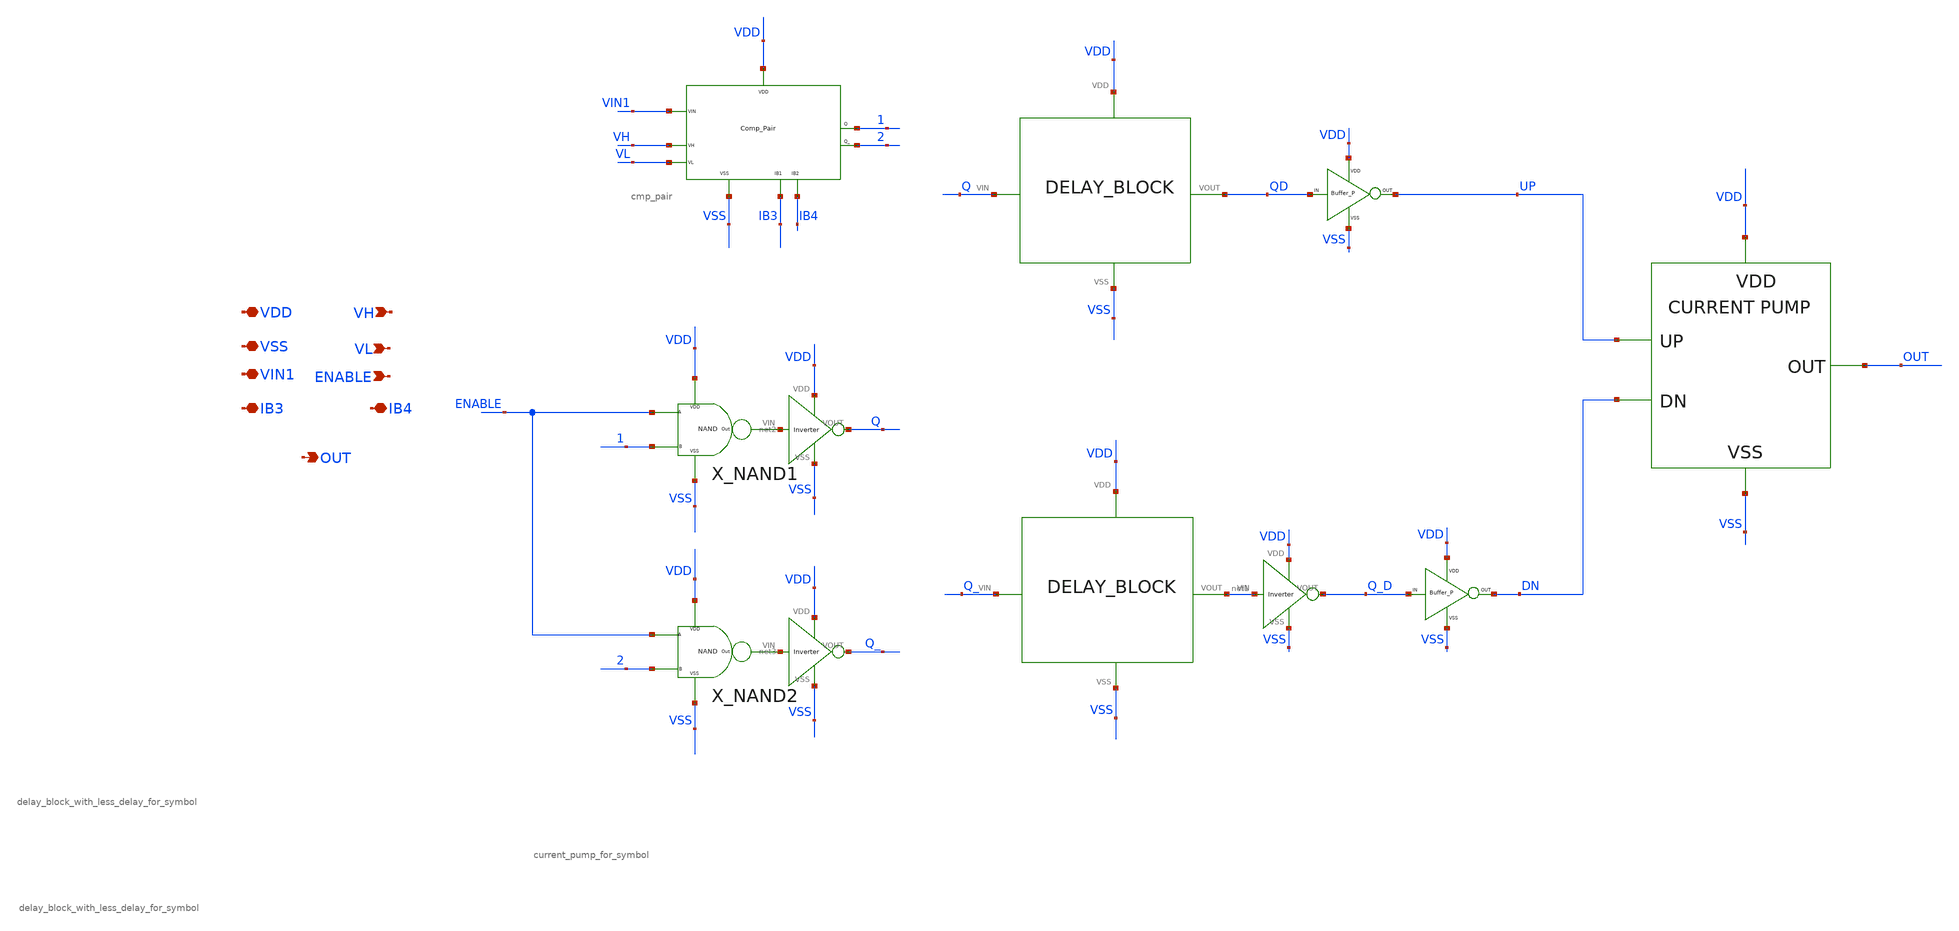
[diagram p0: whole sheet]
** sch_path: xschem/DC_DC_Converter_xschem/OTHERS/DC_DC_Converter_JV11/TOP_LEVEL/Top_Final/Top_2.sch
**.subckt Top_2 VDD VSS OUT VH VL IB3 IB4 ENABLE VIN1
*.iopin VDD
*.iopin VSS
*.opin OUT
*.ipin VH
*.ipin VL
*.iopin IB3
*.iopin IB4
*.ipin ENABLE
*.iopin VIN1
XM1 VDD VSS VIN1 VH VL IB3 IB4 1 2 cmp_pair
X7 UP OUT VDD VSS DN current_pump_for_symbol
X_NAND1 VDD VSS ENABLE 1 net2 NAND
X_NAND2 VDD VSS ENABLE 2 net3 NAND
X9 VSS VDD net2 Q Inverter
X10 VSS VDD net3 Q_ Inverter
X1 Q QD VDD VSS delay_block_with_less_delay_for_symbol
X2 QD UP VDD VSS BUFFER_P
X3 Q_ net1 VDD VSS delay_block_with_less_delay_for_symbol
X5 Q_D DN VDD VSS BUFFER_P
X8 VSS VDD net1 Q_D Inverter
**.ends
.end
